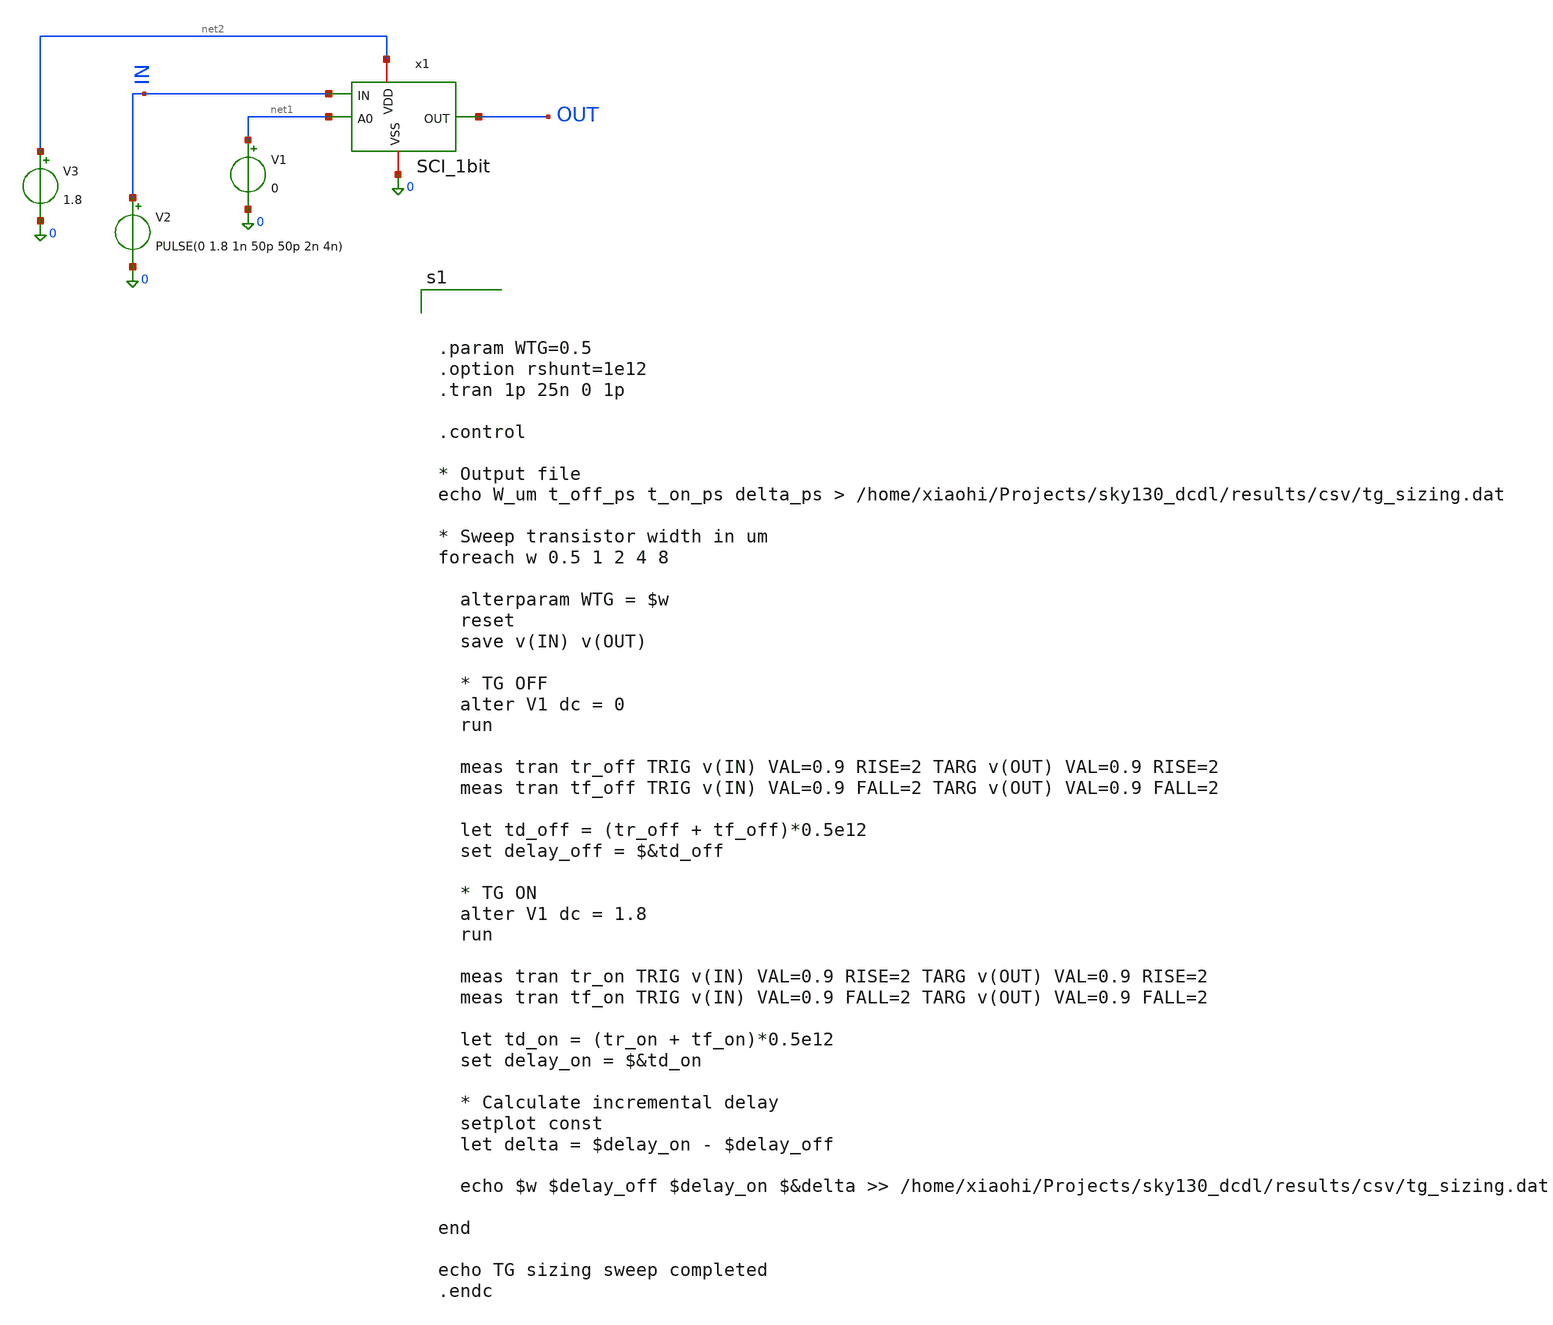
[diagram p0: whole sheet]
** sch_path: xschem/schematic/SCI_DCDL/TG_SCI/TB_TG1BIT.sch
**.subckt TB_TG1BIT
x1 net2 IN OUT 0 net1 SCI_1bit
V1 net1 0 0
V2 IN 0 PULSE(0 1.8 1n 50p 50p 2n 4n)
V3 net2 0 1.8
**** begin user architecture code



.param WTG=0.5
.option rshunt=1e12
.tran 1p 25n 0 1p

.control

* Output file
echo W_um t_off_ps t_on_ps delta_ps > /home/xiaohi/Projects/sky130_dcdl/results/csv/tg_sizing.dat

* Sweep transistor width in um
foreach w 0.5 1 2 4 8

  alterparam WTG = $w
  reset
  save v(IN) v(OUT)

  * TG OFF
  alter V1 dc = 0
  run

  meas tran tr_off TRIG v(IN) VAL=0.9 RISE=2 TARG v(OUT) VAL=0.9 RISE=2
  meas tran tf_off TRIG v(IN) VAL=0.9 FALL=2 TARG v(OUT) VAL=0.9 FALL=2

  let td_off = (tr_off + tf_off)*0.5e12
  set delay_off = $&td_off

  * TG ON
  alter V1 dc = 1.8
  run

  meas tran tr_on TRIG v(IN) VAL=0.9 RISE=2 TARG v(OUT) VAL=0.9 RISE=2
  meas tran tf_on TRIG v(IN) VAL=0.9 FALL=2 TARG v(OUT) VAL=0.9 FALL=2

  let td_on = (tr_on + tf_on)*0.5e12
  set delay_on = $&td_on

  * Calculate incremental delay
  setplot const
  let delta = $delay_on - $delay_off

  echo $w $delay_off $delay_on $&delta >>
+ /home/xiaohi/Projects/sky130_dcdl/results/csv/tg_sizing.dat

end

echo TG sizing sweep completed
.endc



** opencircuitdesign pdks install
.lib $::SKYWATER_MODELS/sky130.lib.spice tt

**** end user architecture code
**.ends

* expanding   symbol:  SCI_1bit.sym # of pins=5
** sym_path: xschem/schematic/SCI_DCDL/TG_SCI/SCI_1bit.sym
** sch_path: xschem/schematic/SCI_DCDL/TG_SCI/SCI_1bit.sch
.subckt SCI_1bit VDD IN OUT VSS A0
*.ipin IN
*.opin OUT
*.iopin VDD
*.iopin VSS
*.ipin A0
XM1 net1 IN VSS VSS sky130_fd_pr__nfet_01v8 L=0.15 W=1 nf=1 ad='int((1 + 1)/2) * 1 / 1 * 0.29' as='int((1 + 2)/2) * 1 / 1 * 0.29'
+ pd='2*int((1 + 1)/2) * (1 / 1 + 0.29)' ps='2*int((1 + 2)/2) * (1 / 1 + 0.29)' nrd='0.29 / 1 ' nrs='0.29 / 1 '
+ sa=0 sb=0 sd=0 mult=1 m=1
XM3 OUT net1 VSS VSS sky130_fd_pr__nfet_01v8 L=0.15 W=1 nf=1 ad='int((1 + 1)/2) * 1 / 1 * 0.29' as='int((1 + 2)/2) * 1 / 1 * 0.29'
+ pd='2*int((1 + 1)/2) * (1 / 1 + 0.29)' ps='2*int((1 + 2)/2) * (1 / 1 + 0.29)' nrd='0.29 / 1 ' nrs='0.29 / 1 '
+ sa=0 sb=0 sd=0 mult=1 m=1
XM5 net1 IN VDD VDD sky130_fd_pr__pfet_01v8 L=0.15 W=2.5 nf=1 ad='int((1 + 1)/2) * 2.5 / 1 * 0.29' as='int((1 + 2)/2) * 2.5 / 1 * 0.29'
+ pd='2*int((1 + 1)/2) * (2.5 / 1 + 0.29)' ps='2*int((1 + 2)/2) * (2.5 / 1 + 0.29)' nrd='0.29 / 2.5 ' nrs='0.29 / 2.5 '
+ sa=0 sb=0 sd=0 mult=1 m=1
XM2 OUT net1 VDD VDD sky130_fd_pr__pfet_01v8 L=0.15 W=2.5 nf=1 ad='int((1 + 1)/2) * 2.5 / 1 * 0.29' as='int((1 + 2)/2) * 2.5 / 1 * 0.29'
+ pd='2*int((1 + 1)/2) * (2.5 / 1 + 0.29)' ps='2*int((1 + 2)/2) * (2.5 / 1 + 0.29)' nrd='0.29 / 2.5 ' nrs='0.29 / 2.5 '
+ sa=0 sb=0 sd=0 mult=1 m=1
XM4 net1 A0 net2 VSS sky130_fd_pr__nfet_01v8 L=0.15 W={WTG} nf=1 ad='int((1 + 1)/2) * {WTG} / 1 * 0.29'
+ as='int((1 + 2)/2) * {WTG} / 1 * 0.29' pd='2*int((1 + 1)/2) * ({WTG} / 1 + 0.29)' ps='2*int((1 + 2)/2) * ({WTG} / 1 + 0.29)'
+ nrd='0.29 / {WTG} ' nrs='0.29 / {WTG} ' sa=0 sb=0 sd=0 mult=1 m=1
XM10 net1 net3 net2 VDD sky130_fd_pr__pfet_01v8 L=0.15 W={WTG} nf=1 ad='int((1 + 1)/2) * {WTG} / 1 * 0.29'
+ as='int((1 + 2)/2) * {WTG} / 1 * 0.29' pd='2*int((1 + 1)/2) * ({WTG} / 1 + 0.29)' ps='2*int((1 + 2)/2) * ({WTG} / 1 + 0.29)'
+ nrd='0.29 / {WTG} ' nrs='0.29 / {WTG} ' sa=0 sb=0 sd=0 mult=1 m=1
.ends

.end
